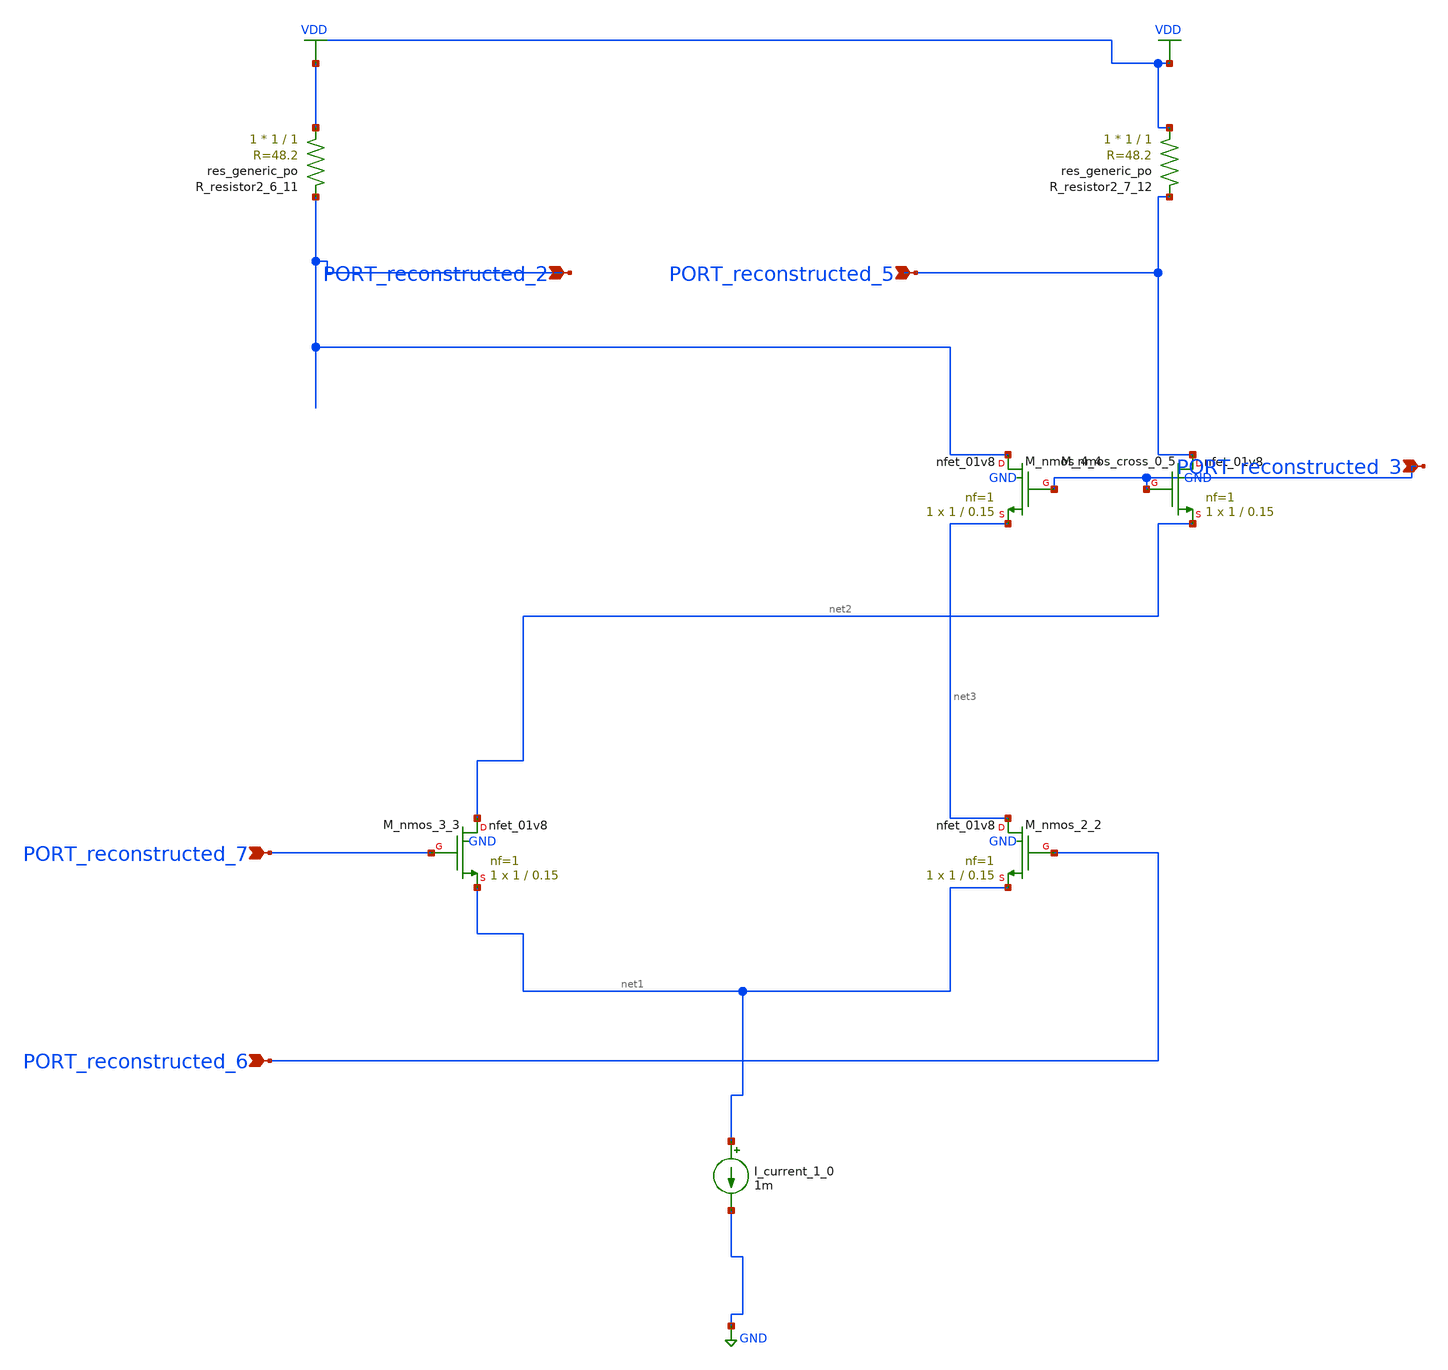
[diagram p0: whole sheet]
** sch_path: schematics/AMSNet/236.sch
**.subckt 236 PORT_reconstructed_3 PORT_reconstructed_6 PORT_reconstructed_2 PORT_reconstructed_5
*+ PORT_reconstructed_7
*.ipin PORT_reconstructed_3
*.ipin PORT_reconstructed_6
*.ipin PORT_reconstructed_2
*.ipin PORT_reconstructed_5
*.ipin PORT_reconstructed_7
I_current_1_0 net1 GND 1m
XM_nmos_2_2 net3 PORT_reconstructed_6 net1 GND sky130_fd_pr__nfet_01v8 L=0.15 W=1 nf=1 ad='int((1 + 1)/2) * 1 / 1 * 0.29'
+ as='int((1 + 2)/2) * 1 / 1 * 0.29' pd='2*int((1 + 1)/2) * (1 / 1 + 0.29)' ps='2*int((1 + 2)/2) * (1 / 1 + 0.29)'
+ nrd='0.29 / 1 ' nrs='0.29 / 1 ' sa=0 sb=0 sd=0 mult=1 m=1
XM_nmos_3_3 net2 PORT_reconstructed_7 net1 GND sky130_fd_pr__nfet_01v8 L=0.15 W=1 nf=1 ad='int((1 + 1)/2) * 1 / 1 * 0.29'
+ as='int((1 + 2)/2) * 1 / 1 * 0.29' pd='2*int((1 + 1)/2) * (1 / 1 + 0.29)' ps='2*int((1 + 2)/2) * (1 / 1 + 0.29)'
+ nrd='0.29 / 1 ' nrs='0.29 / 1 ' sa=0 sb=0 sd=0 mult=1 m=1
XM_nmos_4_4 PORT_reconstructed_2 PORT_reconstructed_3 net3 GND sky130_fd_pr__nfet_01v8 L=0.15 W=1 nf=1
+ ad='int((1 + 1)/2) * 1 / 1 * 0.29' as='int((1 + 2)/2) * 1 / 1 * 0.29' pd='2*int((1 + 1)/2) * (1 / 1 + 0.29)'
+ ps='2*int((1 + 2)/2) * (1 / 1 + 0.29)' nrd='0.29 / 1 ' nrs='0.29 / 1 ' sa=0 sb=0 sd=0 mult=1 m=1
XM_nmos_cross_0_5 PORT_reconstructed_5 PORT_reconstructed_3 net2 GND sky130_fd_pr__nfet_01v8 L=0.15 W=1
+ nf=1 ad='int((1 + 1)/2) * 1 / 1 * 0.29' as='int((1 + 2)/2) * 1 / 1 * 0.29' pd='2*int((1 + 1)/2) * (1 / 1 + 0.29)'
+ ps='2*int((1 + 2)/2) * (1 / 1 + 0.29)' nrd='0.29 / 1 ' nrs='0.29 / 1 ' sa=0 sb=0 sd=0 mult=1 m=1
XR_resistor2_6_11 VDD PORT_reconstructed_2 sky130_fd_pr__res_generic_po W=1 L=1 m=1
XR_resistor2_7_12 VDD PORT_reconstructed_5 sky130_fd_pr__res_generic_po W=1 L=1 m=1
**.ends
.GLOBAL GND
.GLOBAL VDD
.end
